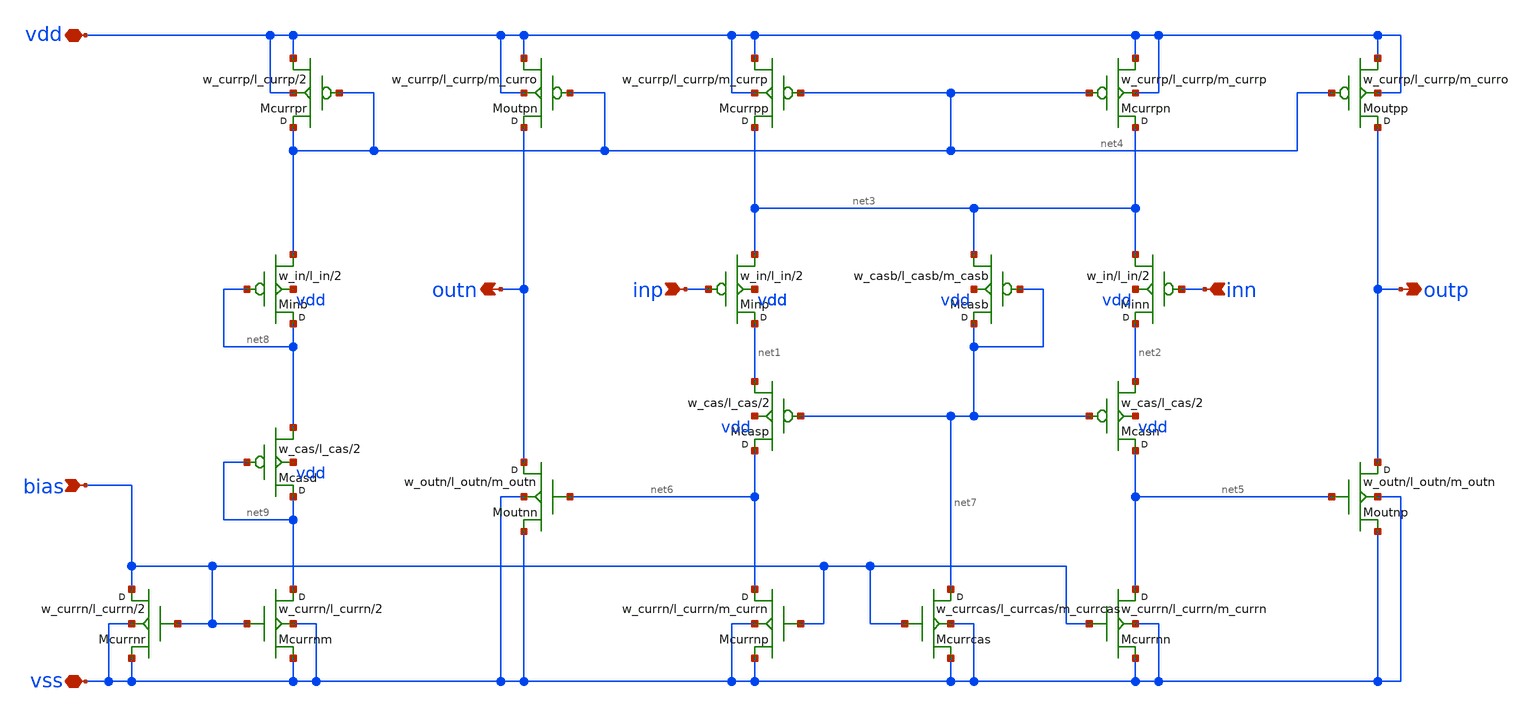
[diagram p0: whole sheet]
** sch_path: design/dac_transz_amp/dac_tranz_amp.sch
**.subckt dac_tranz_amp inp inn outp outn bias vdd vss
*.ipin inp
*.ipin inn
*.opin outp
*.opin outn
*.ipin bias
*.iopin vdd
*.iopin vss
Minp net1 inp net3 vdd pmos w=w_in l=l_in m=2
Minn net2 inn net3 vdd pmos w=w_in l=l_in m=2
Mcasp net6 net7 net1 vdd pmos w=w_cas l=l_cas m=2
Mcasn net5 net7 net2 vdd pmos w=w_cas l=l_cas m=2
Mcurrpp net3 net4 vdd vdd pmos w=w_currp l=l_currp m=m_currp
Mcurrpn net3 net4 vdd vdd pmos w=w_currp l=l_currp m=m_currp
Mcurrnn net5 bias vss vss nmos w=w_currn l=l_currn m=m_currn
Mcurrnp net6 bias vss vss nmos w=w_currn l=l_currn m=m_currn
Moutpp outp net4 vdd vdd pmos w=w_currp l=l_currp m=m_curro
Moutpn outn net4 vdd vdd pmos w=w_currp l=l_currp m=m_curro
Moutnn outn net6 vss vss nmos w=w_outn l=l_outn m=m_outn
Moutnp outp net5 vss vss nmos w=w_outn l=l_outn m=m_outn
Mcurrnm net9 bias vss vss nmos w=w_currn l=l_currn m=2
Mcurrnr bias bias vss vss nmos w=w_currn l=l_currn m=2
Mcurrpr net4 net4 vdd vdd pmos w=w_currp l=l_currp m=2
Minb net8 net8 net4 vdd pmos w=w_in l=l_in m=2
Mcurrcas net7 bias vss vss nmos w=w_currcas l=l_currcas m=m_currcas
Mcasb net7 net7 net3 vdd pmos w=w_casb l=l_casb m=m_casb
Mcasd net9 net9 net8 vdd pmos w=w_cas l=l_cas m=2
**.ends
.end
